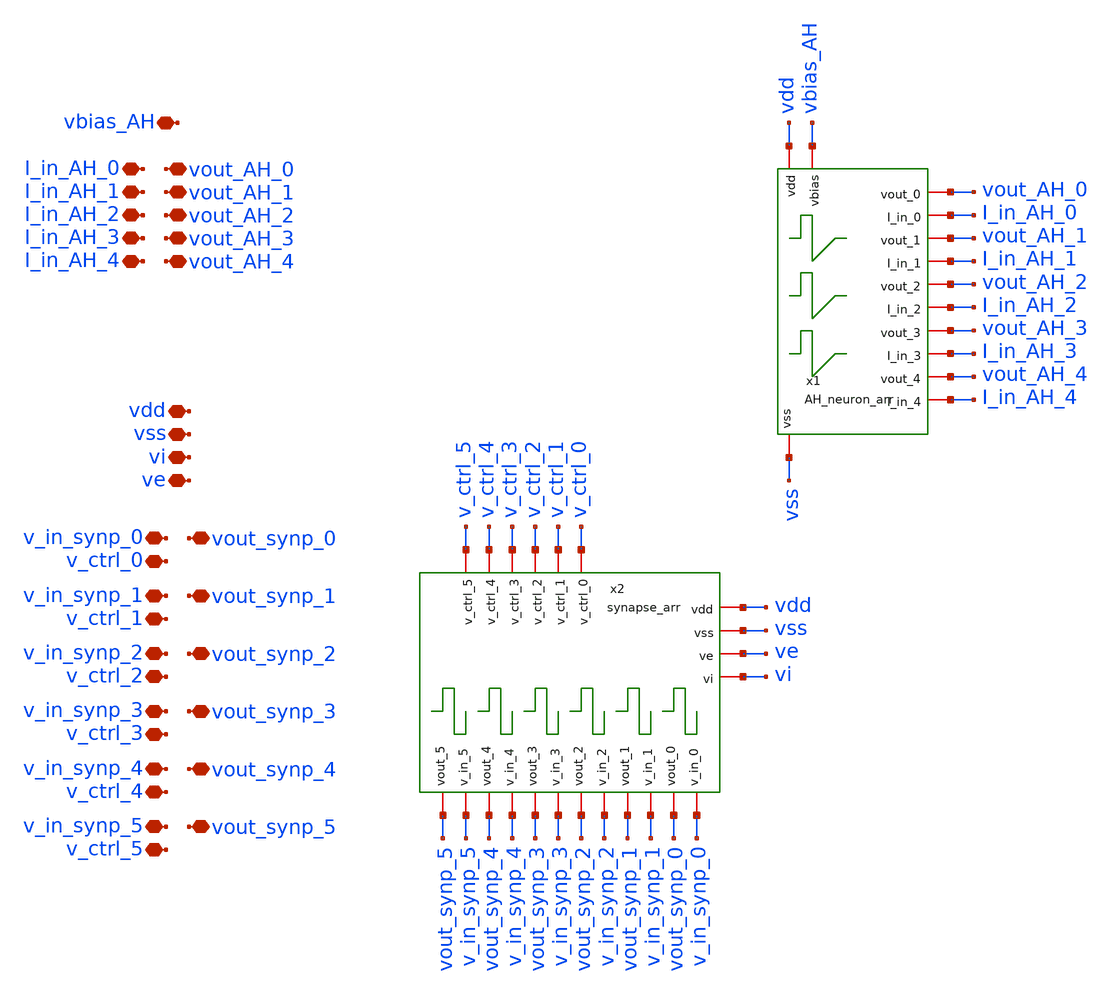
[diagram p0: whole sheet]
** sch_path: designs/libs/core_AH_neuron_arr_synapse_arr/AH_neuron_arr_synapse_arr.sch
**.subckt AH_neuron_arr_synapse_arr I_in_AH_0 vout_AH_0 I_in_AH_1 vout_AH_1 I_in_AH_2 vout_AH_2
*+ I_in_AH_3 vout_AH_3 I_in_AH_4 vout_AH_4 vbias_AH vdd vss v_in_synp_0 vout_synp_0 v_in_synp_1 vout_synp_1
*+ v_in_synp_2 vout_synp_2 v_in_synp_3 vout_synp_3 v_in_synp_4 vout_synp_4 v_in_synp_5 vout_synp_5 v_ctrl_0
*+ v_ctrl_1 v_ctrl_2 v_ctrl_3 v_ctrl_4 v_ctrl_5 vi ve
*.iopin I_in_AH_0
*.iopin vout_AH_0
*.iopin I_in_AH_1
*.iopin vout_AH_1
*.iopin I_in_AH_2
*.iopin vout_AH_2
*.iopin I_in_AH_3
*.iopin vout_AH_3
*.iopin I_in_AH_4
*.iopin vout_AH_4
*.iopin vbias_AH
*.iopin vdd
*.iopin vss
*.iopin v_in_synp_0
*.iopin vout_synp_0
*.iopin v_in_synp_1
*.iopin vout_synp_1
*.iopin v_in_synp_2
*.iopin vout_synp_2
*.iopin v_in_synp_3
*.iopin vout_synp_3
*.iopin v_in_synp_4
*.iopin vout_synp_4
*.iopin v_in_synp_5
*.iopin vout_synp_5
*.iopin v_ctrl_0
*.iopin v_ctrl_1
*.iopin v_ctrl_2
*.iopin v_ctrl_3
*.iopin v_ctrl_4
*.iopin v_ctrl_5
*.iopin vi
*.iopin ve
x1 vdd vss vout_AH_0 I_in_AH_0 I_in_AH_1 vout_AH_1 I_in_AH_2 vout_AH_2 vout_AH_3 I_in_AH_3 vout_AH_4
+ I_in_AH_4 vbias_AH AH_neuron_arr
x2 vdd vss vi ve vout_synp_0 v_in_synp_0 v_ctrl_0 vout_synp_1 v_in_synp_1 v_ctrl_1 v_in_synp_2
+ vout_synp_2 v_ctrl_2 vout_synp_3 v_in_synp_3 v_ctrl_3 vout_synp_4 v_in_synp_4 v_ctrl_4 vout_synp_5 v_in_synp_5
+ v_ctrl_5 synapse_arr
**.ends

* expanding   symbol:  designs/libs/core_AH_neuron_arr/AH_neuron_arr.sym # of pins=13
** sym_path: designs/libs/core_AH_neuron_arr/AH_neuron_arr.sym
** sch_path: designs/libs/core_AH_neuron_arr/AH_neuron_arr.sch
.subckt AH_neuron_arr vdd vss vout_0 I_in_0 I_in_1 vout_1 I_in_2 vout_2 vout_3 I_in_3 vout_4 I_in_4
+ vbias
*.iopin vdd
*.iopin vss
*.iopin I_in_0
*.iopin vout_0
*.iopin I_in_1
*.iopin vout_1
*.iopin I_in_2
*.iopin vout_2
*.iopin I_in_3
*.iopin vout_3
*.iopin I_in_4
*.iopin vout_4
*.iopin vbias
x3 vdd I_in_3 vout_3 vss vbias AH_neuron
x0 vdd I_in_0 vout_0 vss vbias AH_neuron
x1 vdd I_in_1 vout_1 vss vbias AH_neuron
x4 vdd I_in_4 vout_4 vss vbias AH_neuron
x2 vdd I_in_2 vout_2 vss vbias AH_neuron
.ends


* expanding   symbol:  designs/libs/core_synapse_arr/synapse_arr.sym # of pins=22
** sym_path: designs/libs/core_synapse_arr/synapse_arr.sym
** sch_path: designs/libs/core_synapse_arr/synapse_arr.sch
.subckt synapse_arr vdd vss vi ve vout_0 v_in_0 v_ctrl_0 vout_1 v_in_1 v_ctrl_1 v_in_2 vout_2
+ v_ctrl_2 vout_3 v_in_3 v_ctrl_3 vout_4 v_in_4 v_ctrl_4 vout_5 v_in_5 v_ctrl_5
*.iopin vdd
*.iopin vss
*.iopin v_in_0
*.iopin vout_0
*.iopin v_in_1
*.iopin vout_1
*.iopin v_in_2
*.iopin vout_2
*.iopin v_in_3
*.iopin vout_3
*.iopin v_in_4
*.iopin vout_4
*.iopin vi
*.iopin ve
*.iopin v_in_5
*.iopin vout_5
*.iopin v_ctrl_0
*.iopin v_ctrl_1
*.iopin v_ctrl_2
*.iopin v_ctrl_3
*.iopin v_ctrl_4
*.iopin v_ctrl_5
x0 vdd v_in_0 ve v_ctrl_0 vout_0 vi vss synapse
x1 vdd v_in_1 ve v_ctrl_1 vout_1 vi vss synapse
x2 vdd v_in_2 ve v_ctrl_2 vout_2 vi vss synapse
x3 vdd v_in_3 ve v_ctrl_3 vout_3 vi vss synapse
x4 vdd v_in_4 ve v_ctrl_4 vout_4 vi vss synapse
x5 vdd v_in_5 ve v_ctrl_5 vout_5 vi vss synapse
.ends


* expanding   symbol:  designs/libs/core_synapse/synapse.sym # of pins=7
** sym_path: designs/libs/core_synapse/synapse.sym
** sch_path: designs/libs/core_synapse/synapse.sch
.subckt synapse vdd v_in ve v_ctrl v_out vi vss
*.iopin v_out
*.iopin v_ctrl
*.iopin ve
*.iopin vi
*.iopin v_in
*.iopin vdd
*.iopin vss
XM5 net2 net2 vdd vdd pfet_03v3 L=0.28u W=0.42u nf=1 ad='int((nf+1)/2) * W/nf * 0.18u' as='int((nf+2)/2) * W/nf * 0.18u'
+ pd='2*int((nf+1)/2) * (W/nf + 0.18u)' ps='2*int((nf+2)/2) * (W/nf + 0.18u)' nrd='0.18u / W' nrs='0.18u / W'
+ sa=0 sb=0 sd=0 m=1
XM1 net1 v_in vdd vdd pfet_03v3 L=0.28u W=0.42u nf=1 ad='int((nf+1)/2) * W/nf * 0.18u' as='int((nf+2)/2) * W/nf * 0.18u'
+ pd='2*int((nf+1)/2) * (W/nf + 0.18u)' ps='2*int((nf+2)/2) * (W/nf + 0.18u)' nrd='0.18u / W' nrs='0.18u / W'
+ sa=0 sb=0 sd=0 m=1
XM3 net1 v_in vss vss nfet_03v3 L=0.28u W=0.42u nf=1 ad='int((nf+1)/2) * W/nf * 0.18u' as='int((nf+2)/2) * W/nf * 0.18u'
+ pd='2*int((nf+1)/2) * (W/nf + 0.18u)' ps='2*int((nf+2)/2) * (W/nf + 0.18u)' nrd='0.18u / W' nrs='0.18u / W'
+ sa=0 sb=0 sd=0 m=1
XM4 net2 v_in net3 vss nfet_03v3 L=0.28u W=0.42u nf=1 ad='int((nf+1)/2) * W/nf * 0.18u' as='int((nf+2)/2) * W/nf * 0.18u'
+ pd='2*int((nf+1)/2) * (W/nf + 0.18u)' ps='2*int((nf+2)/2) * (W/nf + 0.18u)' nrd='0.18u / W' nrs='0.18u / W'
+ sa=0 sb=0 sd=0 m=1
XM6 net3 ve vss vss nfet_03v3 L=0.28u W=0.42u nf=1 ad='int((nf+1)/2) * W/nf * 0.18u' as='int((nf+2)/2) * W/nf * 0.18u'
+ pd='2*int((nf+1)/2) * (W/nf + 0.18u)' ps='2*int((nf+2)/2) * (W/nf + 0.18u)' nrd='0.18u / W' nrs='0.18u / W'
+ sa=0 sb=0 sd=0 m=1
XM7 net5 vi vdd vdd pfet_03v3 L=0.28u W=0.42u nf=1 ad='int((nf+1)/2) * W/nf * 0.18u' as='int((nf+2)/2) * W/nf * 0.18u'
+ pd='2*int((nf+1)/2) * (W/nf + 0.18u)' ps='2*int((nf+2)/2) * (W/nf + 0.18u)' nrd='0.18u / W' nrs='0.18u / W'
+ sa=0 sb=0 sd=0 m=1
XM8 net4 net1 net5 vdd pfet_03v3 L=0.28u W=0.42u nf=1 ad='int((nf+1)/2) * W/nf * 0.18u' as='int((nf+2)/2) * W/nf * 0.18u'
+ pd='2*int((nf+1)/2) * (W/nf + 0.18u)' ps='2*int((nf+2)/2) * (W/nf + 0.18u)' nrd='0.18u / W' nrs='0.18u / W'
+ sa=0 sb=0 sd=0 m=1
XM9 net4 net4 vss vss nfet_03v3 L=0.28u W=0.42u nf=1 ad='int((nf+1)/2) * W/nf * 0.18u' as='int((nf+2)/2) * W/nf * 0.18u'
+ pd='2*int((nf+1)/2) * (W/nf + 0.18u)' ps='2*int((nf+2)/2) * (W/nf + 0.18u)' nrd='0.18u / W' nrs='0.18u / W'
+ sa=0 sb=0 sd=0 m=1
XM2 net7 net2 vdd vdd pfet_03v3 L=0.28u W=2.8u nf=1 ad='int((nf+1)/2) * W/nf * 0.18u' as='int((nf+2)/2) * W/nf * 0.18u'
+ pd='2*int((nf+1)/2) * (W/nf + 0.18u)' ps='2*int((nf+2)/2) * (W/nf + 0.18u)' nrd='0.18u / W' nrs='0.18u / W'
+ sa=0 sb=0 sd=0 m=1
XM10 v_out v_ctrl net7 vdd pfet_03v3 L=0.28u W=2.8u nf=1 ad='int((nf+1)/2) * W/nf * 0.18u' as='int((nf+2)/2) * W/nf * 0.18u'
+ pd='2*int((nf+1)/2) * (W/nf + 0.18u)' ps='2*int((nf+2)/2) * (W/nf + 0.18u)' nrd='0.18u / W' nrs='0.18u / W'
+ sa=0 sb=0 sd=0 m=1
XM11 v_out v_ctrl net6 vss nfet_03v3 L=0.28u W=2u nf=1 ad='int((nf+1)/2) * W/nf * 0.18u' as='int((nf+2)/2) * W/nf * 0.18u'
+ pd='2*int((nf+1)/2) * (W/nf + 0.18u)' ps='2*int((nf+2)/2) * (W/nf + 0.18u)' nrd='0.18u / W' nrs='0.18u / W'
+ sa=0 sb=0 sd=0 m=1
XM12 net6 net4 vss vss nfet_03v3 L=0.28u W=1u nf=1 ad='int((nf+1)/2) * W/nf * 0.18u' as='int((nf+2)/2) * W/nf * 0.18u'
+ pd='2*int((nf+1)/2) * (W/nf + 0.18u)' ps='2*int((nf+2)/2) * (W/nf + 0.18u)' nrd='0.18u / W' nrs='0.18u / W'
+ sa=0 sb=0 sd=0 m=1
.ends

.end
